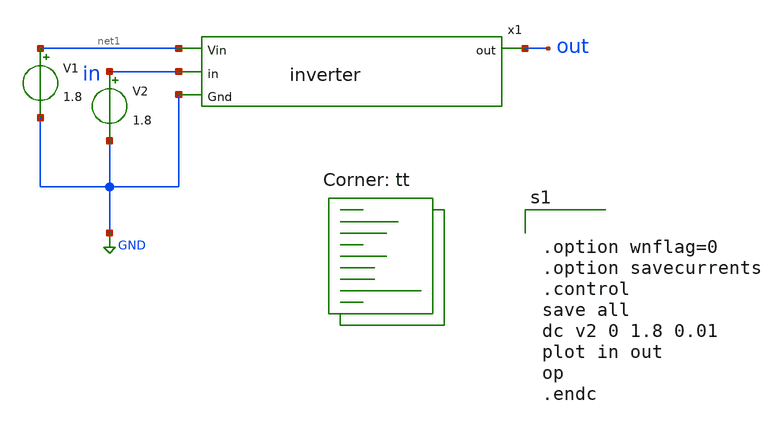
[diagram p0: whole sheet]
** sch_path: Inverter-Ringoscillator/inverter_simulation.sch
**.subckt inverter_simulation
x1 net1 in out GND inverter
V1 net1 GND 1.8
V2 in GND 1.8
**** begin user architecture code
.lib $::SKYWATER_MODELS/sky130.lib.spice tt


.option wnflag=0
.option savecurrents
.control
save all
dc v2 0 1.8 0.01
plot in out
op
.endc


**** end user architecture code
**.ends

* expanding   symbol:  inverter.sym # of pins=4
** sym_path: Inverter-Ringoscillator/inverter.sym
** sch_path: Inverter-Ringoscillator/inverter.sch
.subckt inverter Vin in out Gnd
*.ipin in
*.ipin Vin
*.ipin Gnd
*.opin out
XM1 out in Gnd Gnd sky130_fd_pr__nfet_01v8 L=0.15 W=1 nf=1 ad='int((nf+1)/2) * W/nf * 0.29' as='int((nf+2)/2) * W/nf * 0.29'
+ pd='2*int((nf+1)/2) * (W/nf + 0.29)' ps='2*int((nf+2)/2) * (W/nf + 0.29)' nrd='0.29 / W' nrs='0.29 / W'
+ sa=0 sb=0 sd=0 mult=1 m=1
XM2 out in Vin Vin sky130_fd_pr__pfet_01v8 L=0.15 W=1 nf=1 ad='int((nf+1)/2) * W/nf * 0.29' as='int((nf+2)/2) * W/nf * 0.29'
+ pd='2*int((nf+1)/2) * (W/nf + 0.29)' ps='2*int((nf+2)/2) * (W/nf + 0.29)' nrd='0.29 / W' nrs='0.29 / W'
+ sa=0 sb=0 sd=0 mult=1 m=1
.ends

.GLOBAL GND
.end
